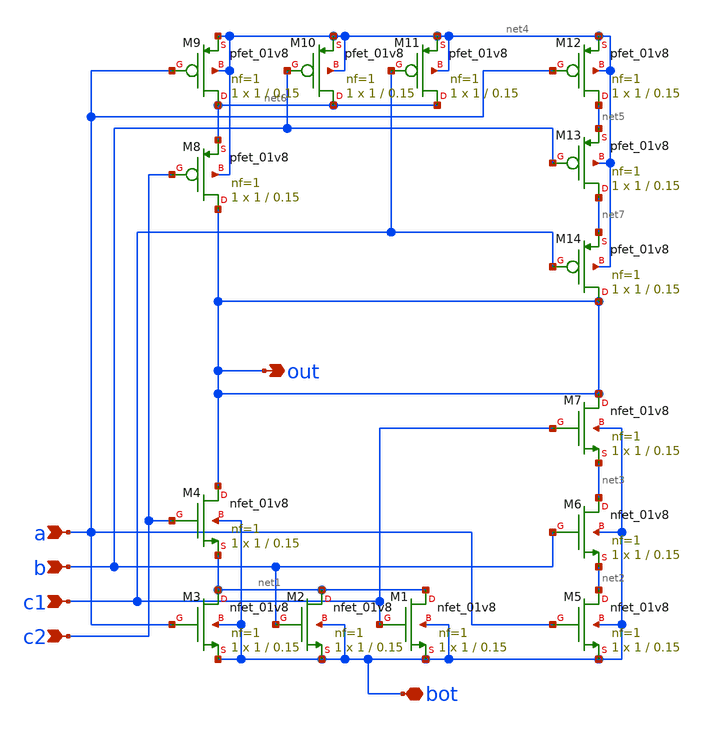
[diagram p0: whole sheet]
** sch_path: tut6/sim/pre_layout/incr/msym-fa-sum-pdn.sch
**.subckt msym-fa-sum-pdn out a b c1 c2 bot
*.opin out
*.ipin a
*.ipin b
*.ipin c1
*.ipin c2
*.iopin bot
XM1 net1 c1 bot bot sky130_fd_pr__nfet_01v8 L=0.15 W=1 nf=1 ad='int((nf+1)/2) * W/nf * 0.29' as='int((nf+2)/2) * W/nf * 0.29'
+ pd='2*int((nf+1)/2) * (W/nf + 0.29)' ps='2*int((nf+2)/2) * (W/nf + 0.29)' nrd='0.29 / W' nrs='0.29 / W'
+ sa=0 sb=0 sd=0 mult=1 m=1
XM2 net1 b bot bot sky130_fd_pr__nfet_01v8 L=0.15 W=1 nf=1 ad='int((nf+1)/2) * W/nf * 0.29' as='int((nf+2)/2) * W/nf * 0.29'
+ pd='2*int((nf+1)/2) * (W/nf + 0.29)' ps='2*int((nf+2)/2) * (W/nf + 0.29)' nrd='0.29 / W' nrs='0.29 / W'
+ sa=0 sb=0 sd=0 mult=1 m=1
XM3 net1 a bot bot sky130_fd_pr__nfet_01v8 L=0.15 W=1 nf=1 ad='int((nf+1)/2) * W/nf * 0.29' as='int((nf+2)/2) * W/nf * 0.29'
+ pd='2*int((nf+1)/2) * (W/nf + 0.29)' ps='2*int((nf+2)/2) * (W/nf + 0.29)' nrd='0.29 / W' nrs='0.29 / W'
+ sa=0 sb=0 sd=0 mult=1 m=1
XM4 out c2 net1 bot sky130_fd_pr__nfet_01v8 L=0.15 W=1 nf=1 ad='int((nf+1)/2) * W/nf * 0.29' as='int((nf+2)/2) * W/nf * 0.29'
+ pd='2*int((nf+1)/2) * (W/nf + 0.29)' ps='2*int((nf+2)/2) * (W/nf + 0.29)' nrd='0.29 / W' nrs='0.29 / W'
+ sa=0 sb=0 sd=0 mult=1 m=1
XM5 net2 a bot bot sky130_fd_pr__nfet_01v8 L=0.15 W=1 nf=1 ad='int((nf+1)/2) * W/nf * 0.29' as='int((nf+2)/2) * W/nf * 0.29'
+ pd='2*int((nf+1)/2) * (W/nf + 0.29)' ps='2*int((nf+2)/2) * (W/nf + 0.29)' nrd='0.29 / W' nrs='0.29 / W'
+ sa=0 sb=0 sd=0 mult=1 m=1
XM6 net3 b net2 bot sky130_fd_pr__nfet_01v8 L=0.15 W=1 nf=1 ad='int((nf+1)/2) * W/nf * 0.29' as='int((nf+2)/2) * W/nf * 0.29'
+ pd='2*int((nf+1)/2) * (W/nf + 0.29)' ps='2*int((nf+2)/2) * (W/nf + 0.29)' nrd='0.29 / W' nrs='0.29 / W'
+ sa=0 sb=0 sd=0 mult=1 m=1
XM7 out c1 net3 bot sky130_fd_pr__nfet_01v8 L=0.15 W=1 nf=1 ad='int((nf+1)/2) * W/nf * 0.29' as='int((nf+2)/2) * W/nf * 0.29'
+ pd='2*int((nf+1)/2) * (W/nf + 0.29)' ps='2*int((nf+2)/2) * (W/nf + 0.29)' nrd='0.29 / W' nrs='0.29 / W'
+ sa=0 sb=0 sd=0 mult=1 m=1
XM8 out c2 net6 net4 sky130_fd_pr__pfet_01v8 L=0.15 W=1 nf=1 ad='int((nf+1)/2) * W/nf * 0.29' as='int((nf+2)/2) * W/nf * 0.29'
+ pd='2*int((nf+1)/2) * (W/nf + 0.29)' ps='2*int((nf+2)/2) * (W/nf + 0.29)' nrd='0.29 / W' nrs='0.29 / W'
+ sa=0 sb=0 sd=0 mult=1 m=1
XM9 net6 a net4 net4 sky130_fd_pr__pfet_01v8 L=0.15 W=1 nf=1 ad='int((nf+1)/2) * W/nf * 0.29' as='int((nf+2)/2) * W/nf * 0.29'
+ pd='2*int((nf+1)/2) * (W/nf + 0.29)' ps='2*int((nf+2)/2) * (W/nf + 0.29)' nrd='0.29 / W' nrs='0.29 / W'
+ sa=0 sb=0 sd=0 mult=1 m=1
XM10 net6 b net4 net4 sky130_fd_pr__pfet_01v8 L=0.15 W=1 nf=1 ad='int((nf+1)/2) * W/nf * 0.29' as='int((nf+2)/2) * W/nf * 0.29'
+ pd='2*int((nf+1)/2) * (W/nf + 0.29)' ps='2*int((nf+2)/2) * (W/nf + 0.29)' nrd='0.29 / W' nrs='0.29 / W'
+ sa=0 sb=0 sd=0 mult=1 m=1
XM11 net6 c1 net4 net4 sky130_fd_pr__pfet_01v8 L=0.15 W=1 nf=1 ad='int((nf+1)/2) * W/nf * 0.29' as='int((nf+2)/2) * W/nf * 0.29'
+ pd='2*int((nf+1)/2) * (W/nf + 0.29)' ps='2*int((nf+2)/2) * (W/nf + 0.29)' nrd='0.29 / W' nrs='0.29 / W'
+ sa=0 sb=0 sd=0 mult=1 m=1
XM12 net5 a net4 net4 sky130_fd_pr__pfet_01v8 L=0.15 W=1 nf=1 ad='int((nf+1)/2) * W/nf * 0.29' as='int((nf+2)/2) * W/nf * 0.29'
+ pd='2*int((nf+1)/2) * (W/nf + 0.29)' ps='2*int((nf+2)/2) * (W/nf + 0.29)' nrd='0.29 / W' nrs='0.29 / W'
+ sa=0 sb=0 sd=0 mult=1 m=1
XM13 net7 b net5 net4 sky130_fd_pr__pfet_01v8 L=0.15 W=1 nf=1 ad='int((nf+1)/2) * W/nf * 0.29' as='int((nf+2)/2) * W/nf * 0.29'
+ pd='2*int((nf+1)/2) * (W/nf + 0.29)' ps='2*int((nf+2)/2) * (W/nf + 0.29)' nrd='0.29 / W' nrs='0.29 / W'
+ sa=0 sb=0 sd=0 mult=1 m=1
XM14 out c1 net7 net4 sky130_fd_pr__pfet_01v8 L=0.15 W=1 nf=1 ad='int((nf+1)/2) * W/nf * 0.29' as='int((nf+2)/2) * W/nf * 0.29'
+ pd='2*int((nf+1)/2) * (W/nf + 0.29)' ps='2*int((nf+2)/2) * (W/nf + 0.29)' nrd='0.29 / W' nrs='0.29 / W'
+ sa=0 sb=0 sd=0 mult=1 m=1
**.ends
.end
